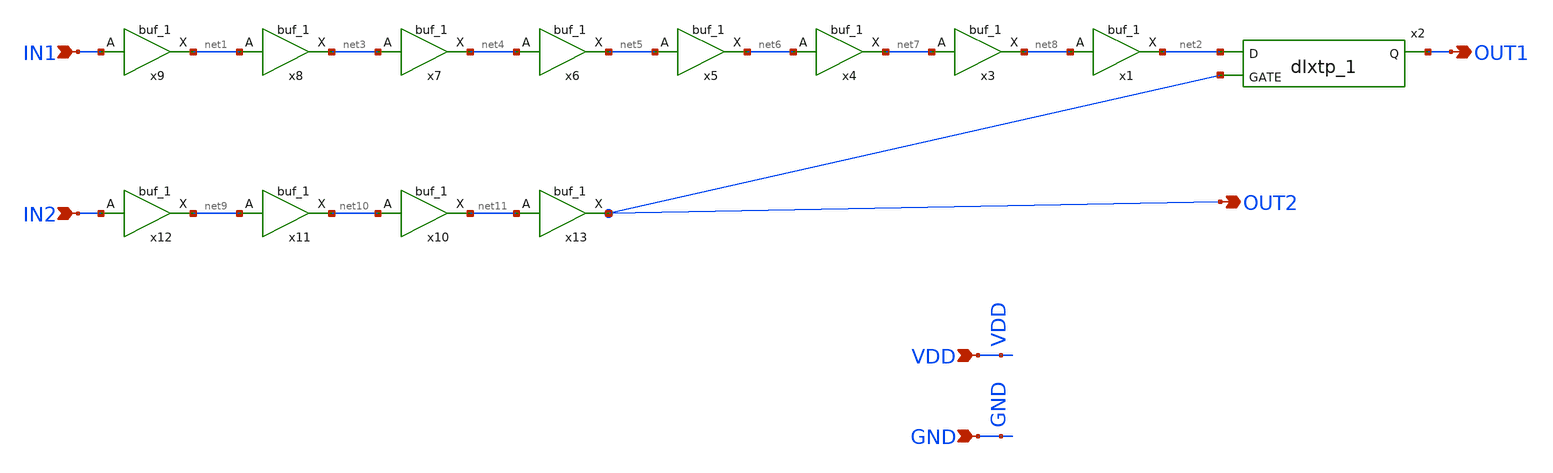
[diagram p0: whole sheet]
** sch_path: xschem/projects/Vernier_Delay_Symbol.sch
**.subckt Vernier_Delay_Symbol VDD GND IN1 IN2 OUT1 OUT2
*.ipin VDD
*.ipin GND
*.ipin IN1
*.ipin IN2
*.opin OUT1
*.opin OUT2
x2 net2 OUT2 0 0 VDD VDD OUT1 sky130_fd_sc_hd__dlxtp_1
x13 net11 GND GND VDD VDD OUT2 sky130_fd_sc_hd__buf_1
x10 net10 GND GND VDD VDD net11 sky130_fd_sc_hd__buf_1
x11 net9 GND GND VDD VDD net10 sky130_fd_sc_hd__buf_1
x12 IN2 GND GND VDD VDD net9 sky130_fd_sc_hd__buf_1
x1 net8 GND GND VDD VDD net2 sky130_fd_sc_hd__buf_1
x3 net7 GND GND VDD VDD net8 sky130_fd_sc_hd__buf_1
x4 net6 GND GND VDD VDD net7 sky130_fd_sc_hd__buf_1
x5 net5 GND GND VDD VDD net6 sky130_fd_sc_hd__buf_1
x6 net4 GND GND VDD VDD net5 sky130_fd_sc_hd__buf_1
x7 net3 GND GND VDD VDD net4 sky130_fd_sc_hd__buf_1
x8 net1 GND GND VDD VDD net3 sky130_fd_sc_hd__buf_1
x9 IN1 GND GND VDD VDD net1 sky130_fd_sc_hd__buf_1
**.ends
.end
